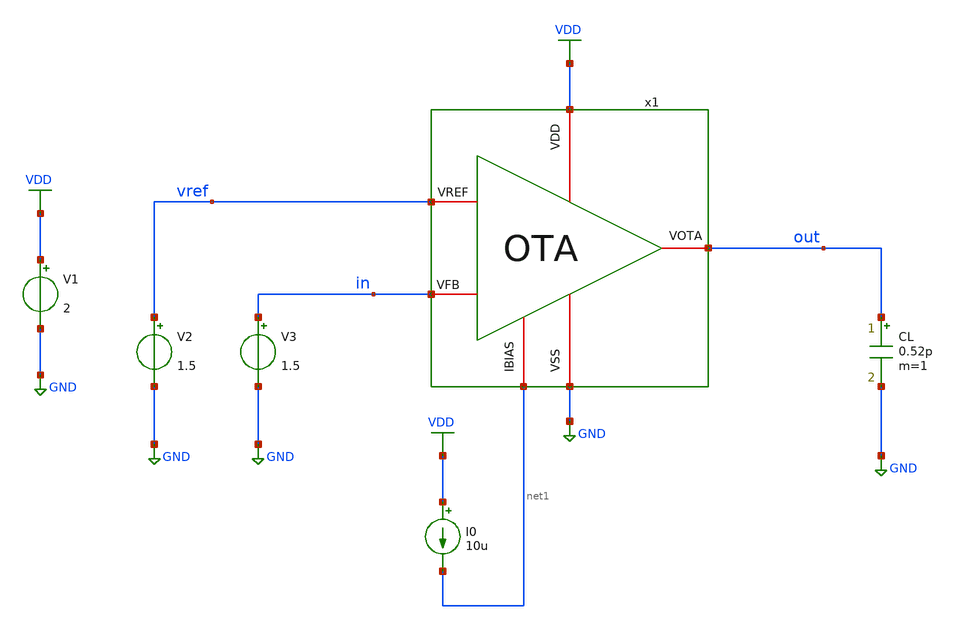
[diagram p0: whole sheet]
** sch_path: designs/libs/tb_ldo/tb_ldo/tb_ldo_OTA/tb_ldo_OTA_tran/tb_ldo_OTA_tran.sch
**.subckt tb_ldo_OTA_tran
V1 VDD GND 2
V2 vref GND 1.5
I0 VDD net1 10u
CL out GND 0.52p m=1
V3 in GND 1.5
x1 VDD vref in out net1 GND OTA
**** begin user architecture code

.include $::180MCU_MODELS/design.ngspice
.lib $::180MCU_MODELS/sm141064.ngspice typical
.lib $::180MCU_MODELS/sm141064.ngspice cap_mim
.lib $::180MCU_MODELS/sm141064.ngspice moscap_typical
.lib $::180MCU_MODELS/sm141064.ngspice mimcap_typical
.lib $::180MCU_MODELS/sm141064.ngspice res_typical
* .lib $::180MCU_MODELS/sm141064.ngspice res_statistical
* ngspice commands




.control
save all

** Define input signal
let fsig = 1k
let tper = 1/fsig
let tfr = 0.01*tper
let ton = 0.5*tper-2*tfr

** Define transient params
let tstop = 2*tper
let tstep = 0.001*tper

** Set sources
alter @V3[PULSE] = [ 1.51 1.49 0 $&tfr $&tfr $&ton $&tper 0]

** Simulations
tran $&tstep $&tstop

** Plots
setplot tran1
let vout = v(out)
let vin = v(in)
plot vin
plot vout

write tb_ldo_OTA_tran.raw

.endc
* ngspice commands



**** end user architecture code
**.ends

* expanding   symbol:  libs/core_ldo/ldo/ldo_OTA/OTA.sym # of pins=6
** sym_path: designs/libs/core_ldo/ldo/OTA.sym
** sch_path: designs/libs/core_ldo/ldo/OTA.sch
.subckt OTA VDD VREF VFB VOTA IBIAS VSS
*.iopin VDD
*.iopin VSS
*.iopin VOTA
*.iopin VREF
*.iopin IBIAS
*.iopin VFB
XM3 net2 net2 VDD VDD pfet_05v0 L=2.00u W=8.00u nf=1 ad='int((nf+1)/2) * W/nf * 0.18u' as='int((nf+2)/2) * W/nf * 0.18u'
+ pd='2*int((nf+1)/2) * (W/nf + 0.18u)' ps='2*int((nf+2)/2) * (W/nf + 0.18u)' nrd='0.18u / W' nrs='0.18u / W'
+ sa=0 sb=0 sd=0 m=1
XM4 net3 net3 VDD VDD pfet_05v0 L=2.00u W=8.00u nf=1 ad='int((nf+1)/2) * W/nf * 0.18u' as='int((nf+2)/2) * W/nf * 0.18u'
+ pd='2*int((nf+1)/2) * (W/nf + 0.18u)' ps='2*int((nf+2)/2) * (W/nf + 0.18u)' nrd='0.18u / W' nrs='0.18u / W'
+ sa=0 sb=0 sd=0 m=1
XM5 net4 net2 VDD VDD pfet_05v0 L=2.00u W=8.00u nf=1 ad='int((nf+1)/2) * W/nf * 0.18u' as='int((nf+2)/2) * W/nf * 0.18u'
+ pd='2*int((nf+1)/2) * (W/nf + 0.18u)' ps='2*int((nf+2)/2) * (W/nf + 0.18u)' nrd='0.18u / W' nrs='0.18u / W'
+ sa=0 sb=0 sd=0 m=1
XM6 VOTA net3 VDD VDD pfet_05v0 L=2.00u W=8.00u nf=1 ad='int((nf+1)/2) * W/nf * 0.18u' as='int((nf+2)/2) * W/nf * 0.18u'
+ pd='2*int((nf+1)/2) * (W/nf + 0.18u)' ps='2*int((nf+2)/2) * (W/nf + 0.18u)' nrd='0.18u / W' nrs='0.18u / W'
+ sa=0 sb=0 sd=0 m=2
XM9 IBIAS IBIAS VSS VSS nfet_05v0 L=2.00u W=4.00u nf=1 ad='int((nf+1)/2) * W/nf * 0.18u' as='int((nf+2)/2) * W/nf * 0.18u'
+ pd='2*int((nf+1)/2) * (W/nf + 0.18u)' ps='2*int((nf+2)/2) * (W/nf + 0.18u)' nrd='0.18u / W' nrs='0.18u / W'
+ sa=0 sb=0 sd=0 m=1
XM10 net1 IBIAS VSS VSS nfet_05v0 L=2.00u W=4.00u nf=1 ad='int((nf+1)/2) * W/nf * 0.18u' as='int((nf+2)/2) * W/nf * 0.18u'
+ pd='2*int((nf+1)/2) * (W/nf + 0.18u)' ps='2*int((nf+2)/2) * (W/nf + 0.18u)' nrd='0.18u / W' nrs='0.18u / W'
+ sa=0 sb=0 sd=0 m=1
XM7 net4 net4 VSS VSS nfet_05v0 L=2.00u W=4.00u nf=1 ad='int((nf+1)/2) * W/nf * 0.18u' as='int((nf+2)/2) * W/nf * 0.18u'
+ pd='2*int((nf+1)/2) * (W/nf + 0.18u)' ps='2*int((nf+2)/2) * (W/nf + 0.18u)' nrd='0.18u / W' nrs='0.18u / W'
+ sa=0 sb=0 sd=0 m=1
XM8 VOTA net4 VSS VSS nfet_05v0 L=2.00u W=4.00u nf=1 ad='int((nf+1)/2) * W/nf * 0.18u' as='int((nf+2)/2) * W/nf * 0.18u'
+ pd='2*int((nf+1)/2) * (W/nf + 0.18u)' ps='2*int((nf+2)/2) * (W/nf + 0.18u)' nrd='0.18u / W' nrs='0.18u / W'
+ sa=0 sb=0 sd=0 m=2
XM1 net2 VREF net1 net1 nfet_05v0 L=0.60u W=40.00u nf=1 ad='int((nf+1)/2) * W/nf * 0.18u' as='int((nf+2)/2) * W/nf * 0.18u'
+ pd='2*int((nf+1)/2) * (W/nf + 0.18u)' ps='2*int((nf+2)/2) * (W/nf + 0.18u)' nrd='0.18u / W' nrs='0.18u / W'
+ sa=0 sb=0 sd=0 m=1
XM2 net3 VFB net1 net1 nfet_05v0 L=0.60u W=40.00u nf=1 ad='int((nf+1)/2) * W/nf * 0.18u' as='int((nf+2)/2) * W/nf * 0.18u'
+ pd='2*int((nf+1)/2) * (W/nf + 0.18u)' ps='2*int((nf+2)/2) * (W/nf + 0.18u)' nrd='0.18u / W' nrs='0.18u / W'
+ sa=0 sb=0 sd=0 m=1
.ends

.GLOBAL GND
.GLOBAL VDD
.end
